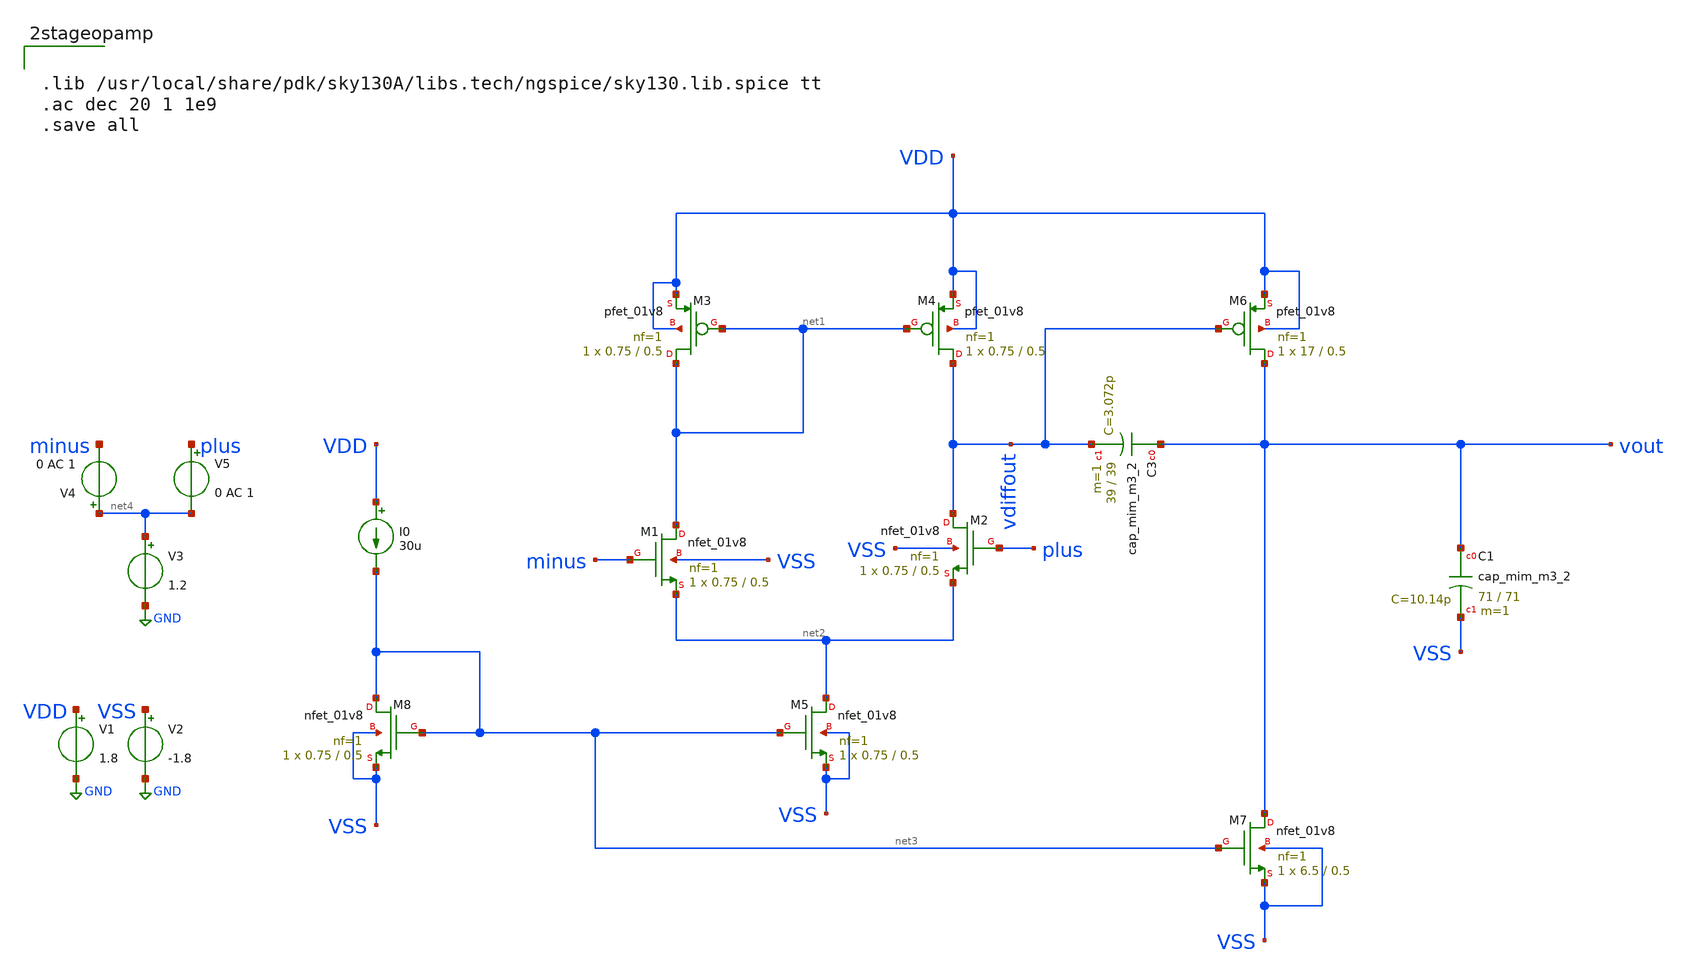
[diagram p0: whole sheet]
** sch_path: xschem/2stageopamptry.sch
**.subckt 2stageopamptry
XM1 net1 minus net2 VSS sky130_fd_pr__nfet_01v8 L=0.5 W=0.75 nf=1 ad='int((nf+1)/2) * W/nf * 0.29' as='int((nf+2)/2) * W/nf * 0.29'
+ pd='2*int((nf+1)/2) * (W/nf + 0.29)' ps='2*int((nf+2)/2) * (W/nf + 0.29)' nrd='0.29 / W' nrs='0.29 / W'
+ sa=0 sb=0 sd=0 mult=1 m=1
XM2 vdiffout plus net2 VSS sky130_fd_pr__nfet_01v8 L=0.5 W=0.75 nf=1 ad='int((nf+1)/2) * W/nf * 0.29'
+ as='int((nf+2)/2) * W/nf * 0.29' pd='2*int((nf+1)/2) * (W/nf + 0.29)' ps='2*int((nf+2)/2) * (W/nf + 0.29)'
+ nrd='0.29 / W' nrs='0.29 / W' sa=0 sb=0 sd=0 mult=1 m=1
XM5 net2 net3 VSS VSS sky130_fd_pr__nfet_01v8 L=0.5 W=0.75 nf=1 ad='int((nf+1)/2) * W/nf * 0.29' as='int((nf+2)/2) * W/nf * 0.29'
+ pd='2*int((nf+1)/2) * (W/nf + 0.29)' ps='2*int((nf+2)/2) * (W/nf + 0.29)' nrd='0.29 / W' nrs='0.29 / W'
+ sa=0 sb=0 sd=0 mult=1 m=1
XM8 net3 net3 VSS VSS sky130_fd_pr__nfet_01v8 L=0.5 W=0.75 nf=1 ad='int((nf+1)/2) * W/nf * 0.29' as='int((nf+2)/2) * W/nf * 0.29'
+ pd='2*int((nf+1)/2) * (W/nf + 0.29)' ps='2*int((nf+2)/2) * (W/nf + 0.29)' nrd='0.29 / W' nrs='0.29 / W'
+ sa=0 sb=0 sd=0 mult=1 m=1
XM7 vout net3 VSS VSS sky130_fd_pr__nfet_01v8 L=0.5 W=6.5 nf=1 ad='int((nf+1)/2) * W/nf * 0.29' as='int((nf+2)/2) * W/nf * 0.29'
+ pd='2*int((nf+1)/2) * (W/nf + 0.29)' ps='2*int((nf+2)/2) * (W/nf + 0.29)' nrd='0.29 / W' nrs='0.29 / W'
+ sa=0 sb=0 sd=0 mult=1 m=1
XM3 net1 net1 VDD VDD sky130_fd_pr__pfet_01v8 L=0.5 W=0.75 nf=1 ad='int((nf+1)/2) * W/nf * 0.29' as='int((nf+2)/2) * W/nf * 0.29'
+ pd='2*int((nf+1)/2) * (W/nf + 0.29)' ps='2*int((nf+2)/2) * (W/nf + 0.29)' nrd='0.29 / W' nrs='0.29 / W'
+ sa=0 sb=0 sd=0 mult=1 m=1
XM4 vdiffout net1 VDD VDD sky130_fd_pr__pfet_01v8 L=0.5 W=0.75 nf=1 ad='int((nf+1)/2) * W/nf * 0.29'
+ as='int((nf+2)/2) * W/nf * 0.29' pd='2*int((nf+1)/2) * (W/nf + 0.29)' ps='2*int((nf+2)/2) * (W/nf + 0.29)'
+ nrd='0.29 / W' nrs='0.29 / W' sa=0 sb=0 sd=0 mult=1 m=1
XM6 vout vdiffout VDD VDD sky130_fd_pr__pfet_01v8 L=0.5 W=17 nf=1 ad='int((nf+1)/2) * W/nf * 0.29' as='int((nf+2)/2) * W/nf * 0.29'
+ pd='2*int((nf+1)/2) * (W/nf + 0.29)' ps='2*int((nf+2)/2) * (W/nf + 0.29)' nrd='0.29 / W' nrs='0.29 / W'
+ sa=0 sb=0 sd=0 mult=1 m=1
I0 VDD net3 30u
V1 VDD GND 1.8
V2 VSS GND -1.8
V4 net4 minus 0 AC 1
V5 plus net4 0 AC 1
V3 net4 GND 1.2
XC3 vout vdiffout sky130_fd_pr__cap_mim_m3_2 W=39 L=39 MF=1 m=1
XC1 vout VSS sky130_fd_pr__cap_mim_m3_2 W=71 L=71 MF=1 m=1
**** begin user architecture code


.lib /usr/local/share/pdk/sky130A/libs.tech/ngspice/sky130.lib.spice tt
.ac dec 20 1 1e9
.save all

**** end user architecture code
**.ends
.GLOBAL GND
.end
